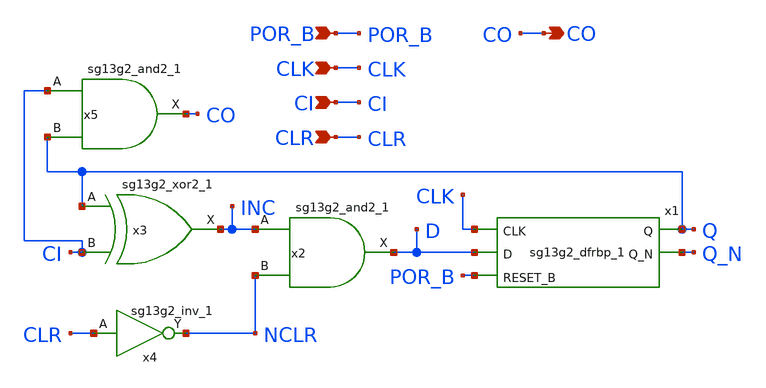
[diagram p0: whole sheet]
** sch_path: design/blocks/counter_bit/schematic/one_bit.sch
**.subckt one_bit CO CLK POR_B CLR CI
*.opin CO
*.ipin CLK
*.ipin POR_B
*.ipin CLR
*.ipin CI
x1 Q Q_N CLK D POR_B VDD VSS sg13g2_dfrbp_1
x2 D INC NCLR VDD VSS sg13g2_and2_1
x3 INC Q CI VDD VSS sg13g2_xor2_1
x4 NCLR CLR VDD VSS sg13g2_inv_1
x5 CO CI Q VDD VSS sg13g2_and2_1
**.ends

* expanding   symbol:  sg13g2_dfrbp_1.sym # of pins=5
** sym_path: sg13g2_dfrbp_1.sym
** sch_path: sg13g2_dfrbp_1.sch
.subckt sg13g2_dfrbp_1 Q Q_N CLK D RESET_B VDD VSS
*.ipin D
*.ipin RESET_B
*.ipin CLK
*.opin Q
*.opin Q_N
*.iopin VDD
*.iopin VSS
XM1 Db D net10 VSS sg13_lv_nmos w=420.00n l=130.00n ng=1 m=1 mm_ok=1
XM2 net10 RESET_B VSS VSS sg13_lv_nmos w=420.00n l=130.00n ng=1 m=1 mm_ok=1
XM3 net1 clkneg net9 VSS sg13_lv_nmos w=420.00n l=130.00n ng=1 m=1 mm_ok=1
XM4 net9 net1 VSS VSS sg13_lv_nmos w=420.00n l=130.00n ng=1 m=1 mm_ok=1
XM5 net1 net1 net5 VSS sg13_lv_nmos w=420.00n l=130.00n ng=1 m=1 mm_ok=1
XM6 net5 RESET_B VSS VSS sg13_lv_nmos w=420.00n l=130.00n ng=1 m=1 mm_ok=1
XM7 Q_N net1 VSS VSS sg13_lv_nmos w=740.00n l=130.00n ng=1 m=1 mm_ok=1
XM8 net2 net1 VSS VSS sg13_lv_nmos w=740.00n l=130.00n ng=1 m=1 mm_ok=1
XM9 Q net2 VSS VSS sg13_lv_nmos w=740.00n l=130.00n ng=1 m=1 mm_ok=1
XM10 clkneg CLK VSS VSS sg13_lv_nmos w=740.00n l=130.00n ng=1 m=1 mm_ok=1
XM11 clkpos clkneg VSS VSS sg13_lv_nmos w=740.00n l=130.00n ng=1 m=1 mm_ok=1
XM12 Db clkneg net3 VSS sg13_lv_nmos w=420.00n l=130.00n ng=1 m=1 mm_ok=1
XM13 net3 clkpos net8 VSS sg13_lv_nmos w=420.00n l=130.00n ng=1 m=1 mm_ok=1
XM14 net8 net3 net4 VSS sg13_lv_nmos w=420.00n l=130.00n ng=1 m=1 mm_ok=1
XM15 net4 RESET_B VSS VSS sg13_lv_nmos w=420.00n l=130.00n ng=1 m=1 mm_ok=1
XM16 net3 net3 VSS VSS sg13_lv_nmos w=740.00n l=130.00n ng=1 m=1 mm_ok=1
XM17 net3 clkpos net1 VSS sg13_lv_nmos w=740.00n l=130.00n ng=1 m=1 mm_ok=1
XM18 Db RESET_B VDD VDD sg13_lv_pmos w=420.00n l=130.00n ng=1 m=1 mm_ok=1
XM19 Db D VDD VDD sg13_lv_pmos w=420.00n l=130.00n ng=1 m=1 mm_ok=1
XM20 net7 net1 VDD VDD sg13_lv_pmos w=420.00n l=130.00n ng=1 m=1 mm_ok=1
XM21 net1 clkpos net7 VDD sg13_lv_pmos w=420.00n l=130.00n ng=1 m=1 mm_ok=1
XM22 net1 net1 VDD VDD sg13_lv_pmos w=420.00n l=130.00n ng=1 m=1 mm_ok=1
XM23 net1 RESET_B VDD VDD sg13_lv_pmos w=420.00n l=130.00n ng=1 m=1 mm_ok=1
XM24 Q_N net1 VDD VDD sg13_lv_pmos w=1.12u l=130.00n ng=1 m=1 mm_ok=1
XM25 net2 net1 VDD VDD sg13_lv_pmos w=1.12u l=130.00n ng=1 m=1 mm_ok=1
XM26 Q net2 VDD VDD sg13_lv_pmos w=1.12u l=130.00n ng=1 m=1 mm_ok=1
XM27 clkneg CLK VDD VDD sg13_lv_pmos w=1.12u l=130.00n ng=1 m=1 mm_ok=1
XM28 clkpos clkneg VDD VDD sg13_lv_pmos w=1.12u l=130.00n ng=1 m=1 mm_ok=1
XM29 Db clkpos net3 VDD sg13_lv_pmos w=420.00n l=130.00n ng=1 m=1 mm_ok=1
XM30 net6 net3 VDD VDD sg13_lv_pmos w=420.00n l=130.00n ng=1 m=1 mm_ok=1
XM31 net3 clkneg net6 VDD sg13_lv_pmos w=420.00n l=130.00n ng=1 m=1 mm_ok=1
XM32 net3 RESET_B VDD VDD sg13_lv_pmos w=420.00n l=130.00n ng=1 m=1 mm_ok=1
XM33 net3 net3 VDD VDD sg13_lv_pmos w=1.000u l=130.00n ng=1 m=1 mm_ok=1
XM34 net3 clkneg net1 VDD sg13_lv_pmos w=1.000u l=130.00n ng=1 m=1 mm_ok=1
.ends


* expanding   symbol:  sg13g2_and2_1.sym # of pins=3
** sym_path: sg13g2_and2_1.sym
** sch_path: sg13g2_and2_1.sch
.subckt sg13g2_and2_1 X A B VDD VSS
*.ipin A
*.ipin B
*.opin X
*.iopin VDD
*.iopin VSS
XM1 net1 A net2 VSS sg13_lv_nmos w=640.00n l=130.00n ng=1 m=1 mm_ok=1
XM2 net2 B VSS VSS sg13_lv_nmos w=640.00n l=130.00n ng=1 m=1 mm_ok=1
XM3 X net1 VSS VSS sg13_lv_nmos w=740.00n l=130.00n ng=1 m=1 mm_ok=1
XM4 net1 B VDD VDD sg13_lv_pmos w=840.00n l=130.00n ng=1 m=1 mm_ok=1
XM5 net1 A VDD VDD sg13_lv_pmos w=840.00n l=130.00n ng=1 m=1 mm_ok=1
XM6 X net1 VDD VDD sg13_lv_pmos w=1.12u l=130.00n ng=1 m=1 mm_ok=1
.ends


* expanding   symbol:  sg13g2_xor2_1.sym # of pins=3
** sym_path: sg13g2_xor2_1.sym
** sch_path: sg13g2_xor2_1.sch
.subckt sg13g2_xor2_1 X A B VDD VSS
*.opin X
*.ipin B
*.ipin A
*.iopin VDD
*.iopin VSS
XM1 net1 A VSS VSS sg13_lv_nmos w=550.00n l=130.00n ng=1 m=1 mm_ok=1
XM2 net1 B VSS VSS sg13_lv_nmos w=550.00n l=130.00n ng=1 m=1 mm_ok=1
XM3 X net1 VSS VSS sg13_lv_nmos w=740.00n l=130.00n ng=1 m=1 mm_ok=1
XM4 X B net3 VSS sg13_lv_nmos w=740.00n l=130.00n ng=1 m=1 mm_ok=1
XM5 net3 A VSS VSS sg13_lv_nmos w=740.00n l=130.00n ng=1 m=1 mm_ok=1
XM6 net4 A VDD VDD sg13_lv_pmos w=1.000u l=130.00n ng=1 m=1 mm_ok=1
XM7 net1 B net4 VDD sg13_lv_pmos w=1.000u l=130.00n ng=1 m=1 mm_ok=1
XM8 net2 A VDD VDD sg13_lv_pmos w=1.12u l=130.00n ng=1 m=1 mm_ok=1
XM9 X net1 net2 VDD sg13_lv_pmos w=1.12u l=130.00n ng=1 m=1 mm_ok=1
XM10 net2 B VDD VDD sg13_lv_pmos w=1.12u l=130.00n ng=1 m=1 mm_ok=1
.ends


* expanding   symbol:  sg13g2_inv_1.sym # of pins=2
** sym_path: sg13g2_inv_1.sym
** sch_path: sg13g2_inv_1.sch
.subckt sg13g2_inv_1 Y A VDD VSS
*.opin Y
*.ipin A
*.iopin VDD
*.iopin VSS
XM1 Y A VSS VSS sg13_lv_nmos w=740.00n l=130.00n ng=1 m=1 mm_ok=1
XM2 Y A VDD VDD sg13_lv_pmos w=1.12u l=130.00n ng=1 m=1 mm_ok=1
.ends

.end
